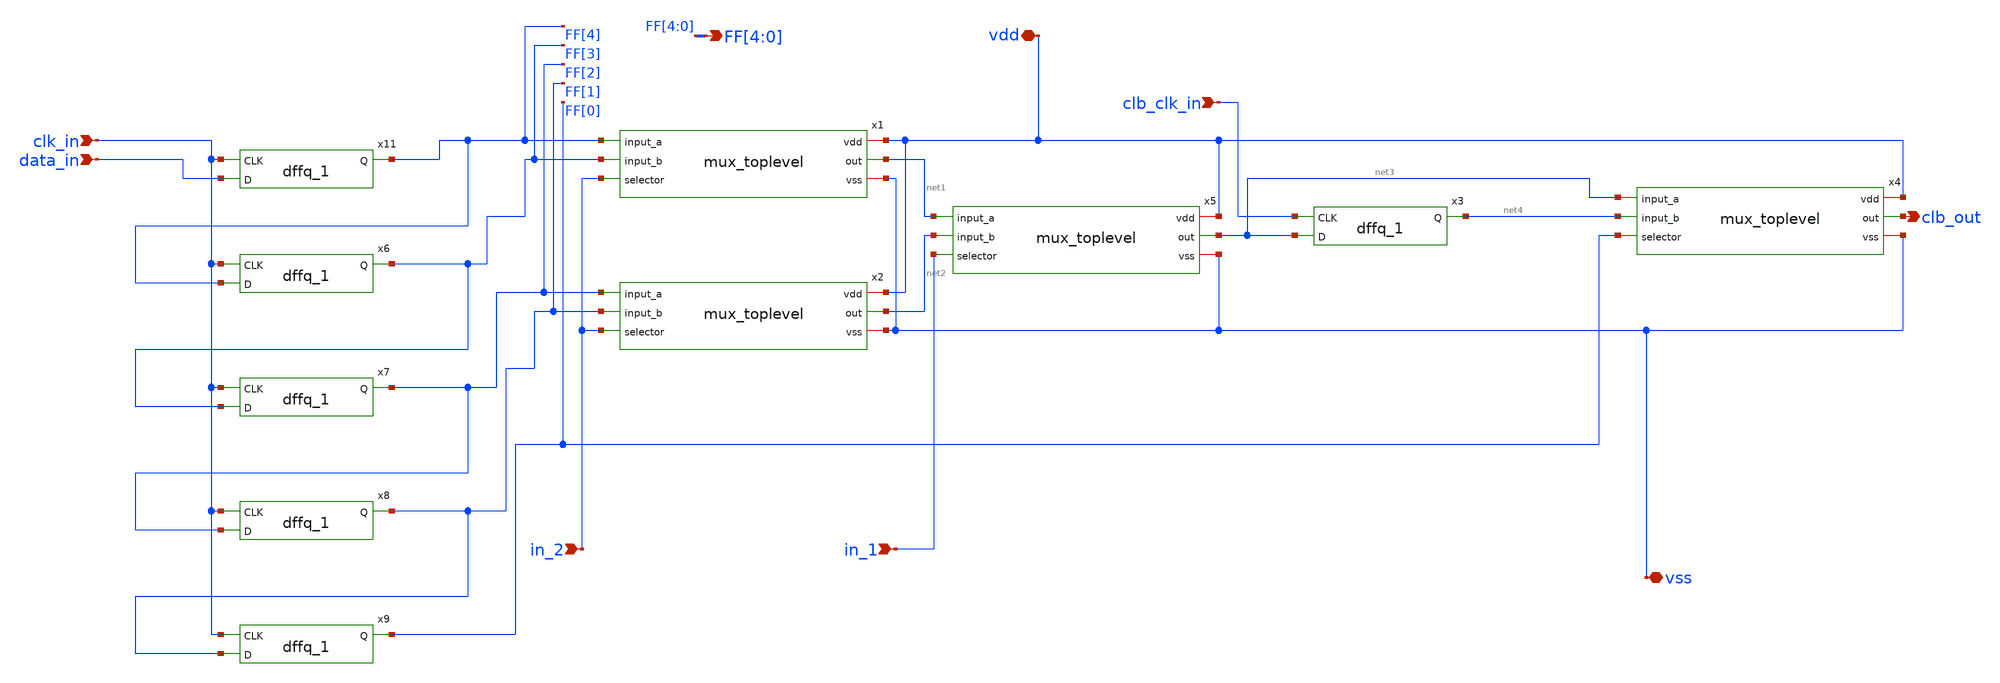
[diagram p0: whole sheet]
** sch_path: designs/libs/core_fpga/clb_2bit/clb_2bit_sc.sch
**.subckt clb_2bit_sc data_in clk_in clb_clk_in vss vdd clb_out in_1 in_2
*+ FF[4],FF[3],FF[2],FF[1],FF[0]
*.ipin data_in
*.ipin clk_in
*.ipin clb_clk_in
*.iopin vss
*.iopin vdd
*.opin clb_out
*.ipin in_1
*.ipin in_2
*.opin FF[4],FF[3],FF[2],FF[1],FF[0]
x1 vdd FF[4] net1 FF[3] in_2 vss mux_toplevel
x2 vdd FF[2] net2 FF[1] in_2 vss mux_toplevel
x5 vdd net1 net3 net2 in_1 vss mux_toplevel
x4 vdd net3 clb_out net4 FF[0] vss mux_toplevel
x11 data_in clk_in FF[4] VDDd VDDd VSSd VSSd gf180mcu_fd_sc_mcu9t5v0__dffq_1
x6 FF[4] clk_in FF[3] VDDd VDDd VSSd VSSd gf180mcu_fd_sc_mcu9t5v0__dffq_1
x7 FF[3] clk_in FF[2] VDDd VDDd VSSd VSSd gf180mcu_fd_sc_mcu9t5v0__dffq_1
x8 FF[2] clk_in FF[1] VDDd VDDd VSSd VSSd gf180mcu_fd_sc_mcu9t5v0__dffq_1
x9 FF[1] clk_in FF[0] VDDd VDDd VSSd VSSd gf180mcu_fd_sc_mcu9t5v0__dffq_1
x3 net3 clb_clk_in net4 VDDd VDDd VSSd VSSd gf180mcu_fd_sc_mcu9t5v0__dffq_1
**.ends
.end
